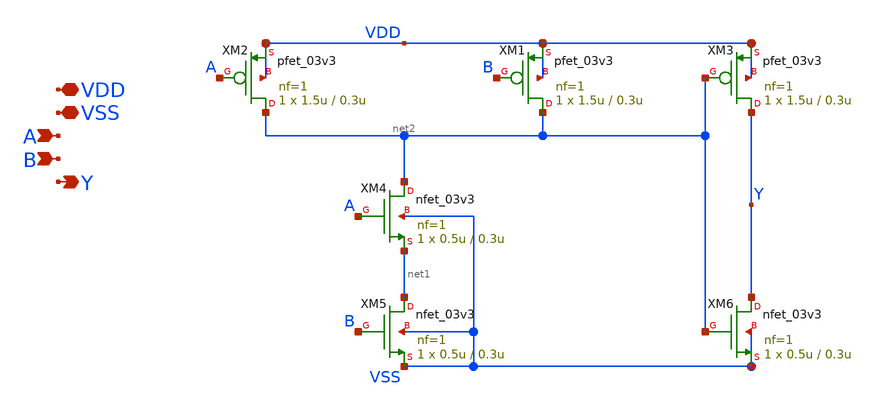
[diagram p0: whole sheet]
** sch_path: designs/libs/core_analog/switch-matrix/and2_1.sch
**.subckt and2_1 VDD VSS A B Y
*.iopin VDD
*.iopin VSS
*.ipin A
*.ipin B
*.opin Y
XM2 net2 A VDD VDD pfet_03v3 L=0.3u W=1.5u nf=1 ad='int((nf+1)/2) * W/nf * 0.18u' as='int((nf+2)/2) * W/nf * 0.18u'
+ pd='2*int((nf+1)/2) * (W/nf + 0.18u)' ps='2*int((nf+2)/2) * (W/nf + 0.18u)' nrd='0.18u / W' nrs='0.18u / W'
+ sa=0 sb=0 sd=0 m=1
XM1 net2 B VDD VDD pfet_03v3 L=0.3u W=1.5u nf=1 ad='int((nf+1)/2) * W/nf * 0.18u' as='int((nf+2)/2) * W/nf * 0.18u'
+ pd='2*int((nf+1)/2) * (W/nf + 0.18u)' ps='2*int((nf+2)/2) * (W/nf + 0.18u)' nrd='0.18u / W' nrs='0.18u / W'
+ sa=0 sb=0 sd=0 m=1
XM3 Y net2 VDD VDD pfet_03v3 L=0.3u W=1.5u nf=1 ad='int((nf+1)/2) * W/nf * 0.18u' as='int((nf+2)/2) * W/nf * 0.18u'
+ pd='2*int((nf+1)/2) * (W/nf + 0.18u)' ps='2*int((nf+2)/2) * (W/nf + 0.18u)' nrd='0.18u / W' nrs='0.18u / W'
+ sa=0 sb=0 sd=0 m=1
XM4 net2 A net1 VSS nfet_03v3 L=0.3u W=0.5u nf=1 ad='int((nf+1)/2) * W/nf * 0.18u' as='int((nf+2)/2) * W/nf * 0.18u'
+ pd='2*int((nf+1)/2) * (W/nf + 0.18u)' ps='2*int((nf+2)/2) * (W/nf + 0.18u)' nrd='0.18u / W' nrs='0.18u / W'
+ sa=0 sb=0 sd=0 m=1
XM5 net1 B VSS VSS nfet_03v3 L=0.3u W=0.5u nf=1 ad='int((nf+1)/2) * W/nf * 0.18u' as='int((nf+2)/2) * W/nf * 0.18u'
+ pd='2*int((nf+1)/2) * (W/nf + 0.18u)' ps='2*int((nf+2)/2) * (W/nf + 0.18u)' nrd='0.18u / W' nrs='0.18u / W'
+ sa=0 sb=0 sd=0 m=1
XM6 Y net2 VSS VSS nfet_03v3 L=0.3u W=0.5u nf=1 ad='int((nf+1)/2) * W/nf * 0.18u' as='int((nf+2)/2) * W/nf * 0.18u'
+ pd='2*int((nf+1)/2) * (W/nf + 0.18u)' ps='2*int((nf+2)/2) * (W/nf + 0.18u)' nrd='0.18u / W' nrs='0.18u / W'
+ sa=0 sb=0 sd=0 m=1
**.ends
.end
